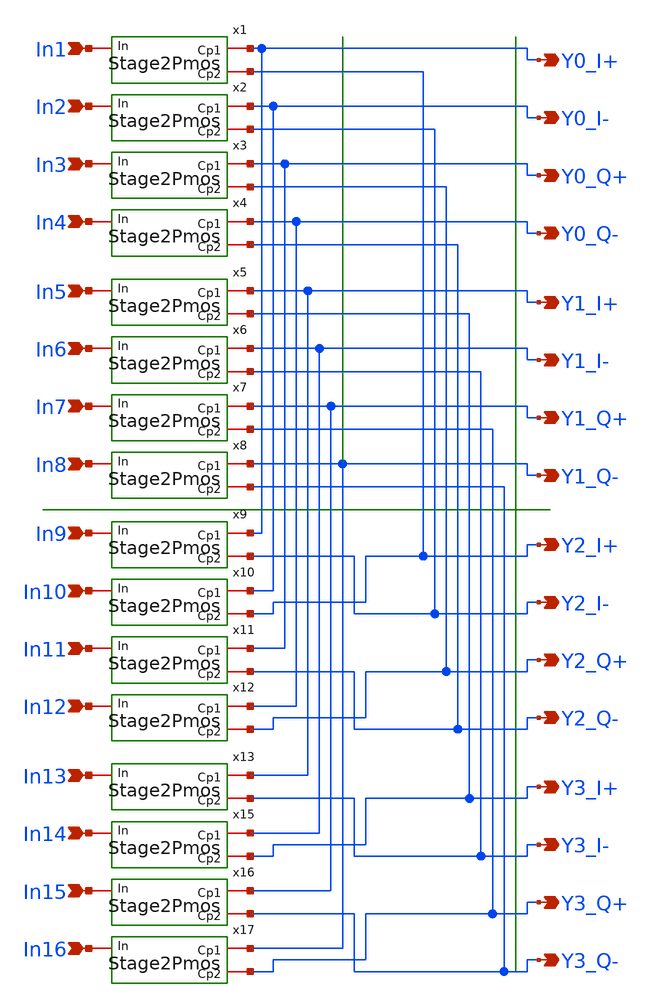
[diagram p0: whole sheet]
** sch_path: xschem/FinalProject/PMOSOutStg.sch
**.subckt PMOSOutStg In1 Y0_I+ In2 Y0_I- In3 Y0_Q+ In4 Y0_Q- In5 Y1_I+ In6 Y1_I- In7 Y1_Q+ In8 Y1_Q-
*+ In9 Y2_I+ In10 In11 Y2_I- Y2_Q+ In12 Y2_Q- In13 Y3_I+ In14 Y3_I- In15 Y3_Q+ In16 Y3_Q-
*.ipin In1
*.opin Y0_I+
*.ipin In2
*.opin Y0_I-
*.ipin In3
*.opin Y0_Q+
*.ipin In4
*.opin Y0_Q-
*.ipin In5
*.opin Y1_I+
*.ipin In6
*.opin Y1_I-
*.ipin In7
*.opin Y1_Q+
*.ipin In8
*.opin Y1_Q-
*.ipin In9
*.opin Y2_I+
*.ipin In10
*.ipin In11
*.opin Y2_I-
*.opin Y2_Q+
*.ipin In12
*.opin Y2_Q-
*.ipin In13
*.opin Y3_I+
*.ipin In14
*.opin Y3_I-
*.ipin In15
*.opin Y3_Q+
*.ipin In16
*.opin Y3_Q-
x1 In1 Y0_I+ Y2_I+ Stage2Pmos
x2 In2 Y0_I- Y2_I- Stage2Pmos
x3 In3 Y0_Q+ Y2_Q+ Stage2Pmos
x4 In4 Y0_Q- Y2_Q- Stage2Pmos
x5 In5 Y1_I+ Y3_I+ Stage2Pmos
x6 In6 Y1_I- Y3_I- Stage2Pmos
x7 In7 Y1_Q+ Y3_Q+ Stage2Pmos
x8 In8 Y1_Q- Y3_Q- Stage2Pmos
x9 In9 Y0_I+ Y2_I- Stage2Pmos
x10 In10 Y0_I- Y2_I+ Stage2Pmos
x11 In11 Y0_Q+ Y2_Q- Stage2Pmos
x12 In12 Y0_Q- Y2_Q+ Stage2Pmos
x13 In13 Y1_I+ Y3_I- Stage2Pmos
x15 In14 Y1_I- Y3_I+ Stage2Pmos
x16 In15 Y1_Q+ Y3_Q- Stage2Pmos
x17 In16 Y1_Q- Y3_Q+ Stage2Pmos
**.ends
.end
